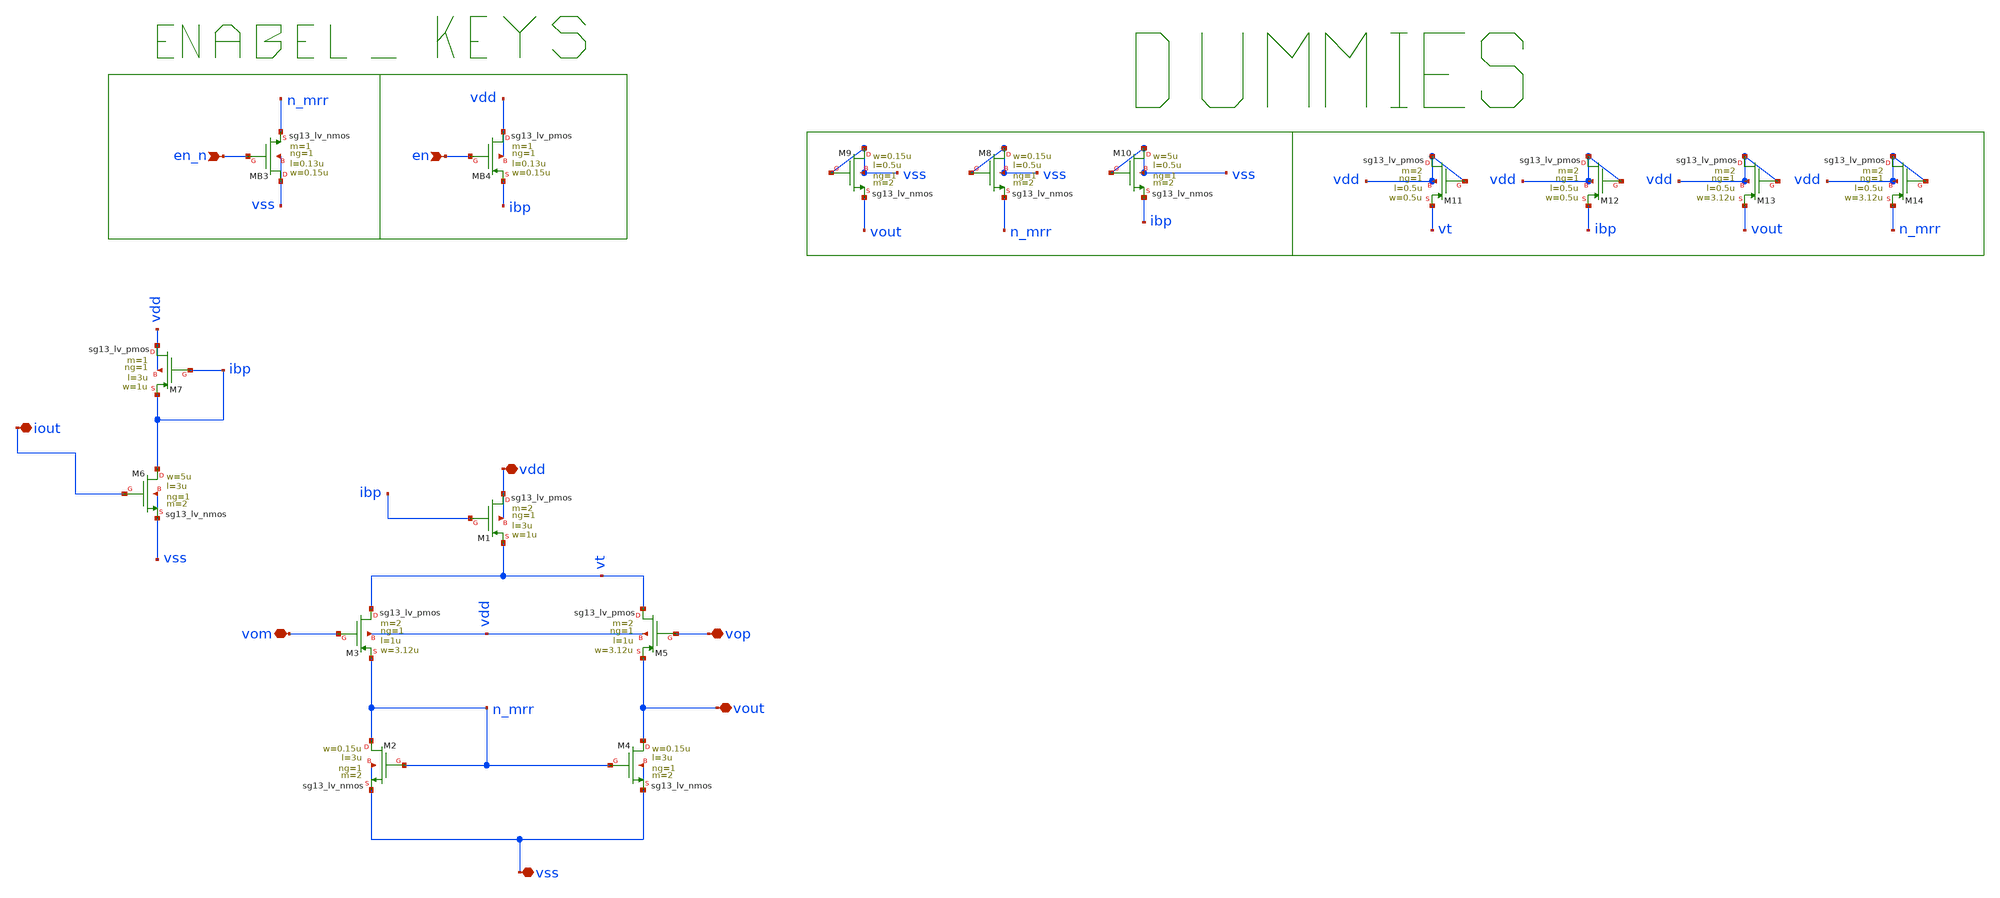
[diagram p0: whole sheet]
** sch_path: schematic/xschem/final_stage_ota/final_stage_ota.sch
**.subckt final_stage_ota vdd vom vop vss vout iout en_n en
*.iopin vdd
*.iopin vom
*.iopin vop
*.iopin vss
*.iopin vout
*.iopin iout
*.ipin en_n
*.ipin en
XM1 vdd ibp vt vdd sg13_lv_pmos w=1u l=3u ng=1 m=2 mm_ok=1
XM2 n_mrr n_mrr vss vss sg13_lv_nmos w=0.15u l=3u ng=1 m=2 mm_ok=1
XM3 vt vom n_mrr vdd sg13_lv_pmos w=3.12u l=1u ng=1 m=2 mm_ok=1
XM4 vout n_mrr vss vss sg13_lv_nmos w=0.15u l=3u ng=1 m=2 mm_ok=1
XM5 vt vop vout vdd sg13_lv_pmos w=3.12u l=1u ng=1 m=2 mm_ok=1
XM6 ibp iout vss vss sg13_lv_nmos w=5u l=3u ng=1 m=2 mm_ok=1
XM7 vdd ibp ibp vdd sg13_lv_pmos w=1u l=3u ng=1 m=1 mm_ok=1
XMB3 vss en_n n_mrr vss sg13_lv_nmos w=0.15u l=0.13u ng=1 m=1 mm_ok=1
XMB4 vdd en ibp vdd sg13_lv_pmos w=0.15u l=0.13u ng=1 m=1 mm_ok=1
XM8 vss vss n_mrr vss sg13_lv_nmos w=0.15u l=0.5u ng=1 m=2 mm_ok=1
XM9 vss vss vout vss sg13_lv_nmos w=0.15u l=0.5u ng=1 m=2 mm_ok=1
XM10 vss vss ibp vss sg13_lv_nmos w=5u l=0.5u ng=1 m=2 mm_ok=1
XM11 vdd vdd vt vdd sg13_lv_pmos w=0.5u l=0.5u ng=1 m=2 mm_ok=1
XM12 vdd vdd ibp vdd sg13_lv_pmos w=0.5u l=0.5u ng=1 m=2 mm_ok=1
XM13 vdd vdd vout vdd sg13_lv_pmos w=3.12u l=0.5u ng=1 m=2 mm_ok=1
XM14 vdd vdd n_mrr vdd sg13_lv_pmos w=3.12u l=0.5u ng=1 m=2 mm_ok=1
**.ends
.end
